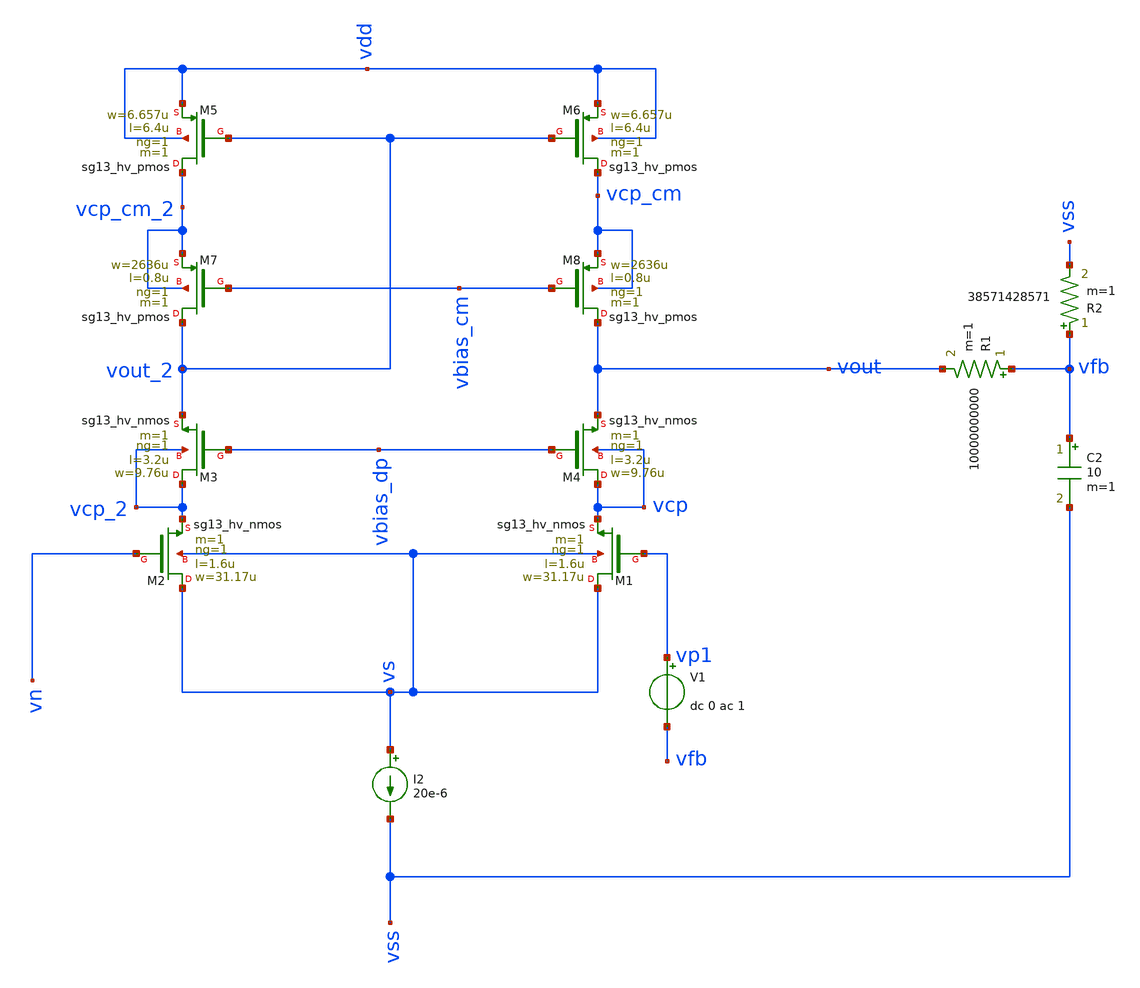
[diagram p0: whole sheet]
** sch_path: test/Tesis_notebooks/xschem/ota_tb_ihp_cc_full.sch
**.subckt ota_tb_ihp_cc_full
I2 vs vss 20e-6
XM1 vs vp1 vcp vs sg13_hv_nmos w=31.17u l=1.6u ng=1 m=1 mm_ok=1
XM2 vs vn vcp_2 vs sg13_hv_nmos w=31.17u l=1.6u ng=1 m=1 mm_ok=1
XM3 vcp_2 vbias_dp vout_2 vcp_2 sg13_hv_nmos w=9.76u l=3.2u ng=1 m=1 mm_ok=1
XM4 vcp vbias_dp vout vcp sg13_hv_nmos w=9.76u l=3.2u ng=1 m=1 mm_ok=1
XM5 vcp_cm_2 vout_2 vdd vdd sg13_hv_pmos w=6.657u l=6.4u ng=1 m=1 mm_ok=1
XM6 vcp_cm vout_2 vdd vdd sg13_hv_pmos w=6.657u l=6.4u ng=1 m=1 mm_ok=1
R1 vfb vout 10000000000 m=1
C2 vfb vss 10 m=1
R2 vfb vss 38571428571 m=1
V1 vp1 vfb dc 0 ac 1
XM7 vout_2 vbias_cm vcp_cm_2 vcp_cm_2 sg13_hv_pmos w=2636u l=0.8u ng=1 m=1 mm_ok=1
XM8 vout vbias_cm vcp_cm vcp_cm sg13_hv_pmos w=2636u l=0.8u ng=1 m=1 mm_ok=1
**** begin user architecture code



.lib /opt/pdks/ihp-sg13g2/libs.tech/ngspice/models/cornerMOShv.lib mos_tt

Vref vn 0 1.35
Vdd vdd 0 3.3
Vbias_dp vbias_dp 0 2.2
Vbias_cm vbias_cm vdd -0.88
Vss vss 0 0

.control
ac dec 10 1 1G



plot vdb(vout)
plot ph(vout)*180/PI
meas ac gain find vdb(vout) at=1
let low_gain = gain-3
meas ac fc WHEN vdb(vout)=low_gain

let phas = ph(vout)*180/PI

meas ac fu WHEN vdb(vout)=0
meas ac pmar find phas at=fu

op

let gm_m1 = @n.xm1.nsg13_hv_nmos[gm]
let gm_m2 = @n.xm2.nsg13_hv_nmos[gm]
let gm_m3 = @n.xm3.nsg13_hv_nmos[gm]
let gm_m4 = @n.xm4.nsg13_hv_nmos[gm]
let gm_m5 = @n.xm5.nsg13_hv_pmos[gm]
let gm_m6 = @n.xm6.nsg13_hv_pmos[gm]
let gm_m7 = @n.xm7.nsg13_hv_pmos[gm]
let gm_m8 = @n.xm8.nsg13_hv_pmos[gm]

let gds_m1 = @n.xm1.nsg13_hv_nmos[gds]
let gds_m2 = @n.xm2.nsg13_hv_nmos[gds]
let gds_m3 = @n.xm3.nsg13_hv_nmos[gds]
let gds_m4 = @n.xm4.nsg13_hv_nmos[gds]
let gds_m5 = @n.xm5.nsg13_hv_pmos[gds]
let gds_m6 = @n.xm6.nsg13_hv_pmos[gds]
let gds_m7 = @n.xm7.nsg13_hv_pmos[gds]
let gds_m8 = @n.xm8.nsg13_hv_pmos[gds]

let cds_m1 = abs(@n.xm1.nsg13_hv_nmos[cds])+abs(@n.xm1.nsg13_hv_nmos[cdb])
let cds_m4 = abs(@n.xm4.nsg13_hv_nmos[cds])+abs(@n.xm4.nsg13_hv_nmos[cdb])
let cds_m6 = abs(@n.xm6.nsg13_hv_pmos[cds])+abs(@n.xm6.nsg13_hv_pmos[cdb])
let cds_m8 = abs(@n.xm8.nsg13_hv_pmos[cds])+abs(@n.xm8.nsg13_hv_pmos[cdb])

let cgd_m1 = @n.xm1.nsg13_hv_nmos[cgd]
let cgd_m4 = @n.xm4.nsg13_hv_nmos[cgd]
let cgd_m6 = @n.xm6.nsg13_hv_pmos[cgd]
let cgd_m8 = @n.xm8.nsg13_hv_pmos[cgd]

let cgs_m1 = @n.xm1.nsg13_hv_nmos[cgg]
let cgs_m4 = @n.xm4.nsg13_hv_nmos[cgg]
let cgs_m6 = @n.xm6.nsg13_hv_pmos[cgg]
let cgs_m8 = @n.xm8.nsg13_hv_pmos[cgg]

let gain_cc1 = (gm_m3/gds_m3)
let gain_cc2 = (gm_m4/gds_m4)

let gain_cc3 = gm_m8/gds_m8
let gain_cc4 = gm_m7/gds_m7

let rout_diff1 = gain_cc1/gds_m1
let rout_diff2 = gain_cc2/gds_m2

let rout_cm1 = gain_cc3/gds_m6
let rout_cm2 = gain_cc4/gds_m5

print vout vs vcp vcp_2 vcp_cm vcp_cm_2 vout_2

print gm_m1
print gm_m2
print gm_m3
print gm_m4
print gm_m5
print gm_m6
print gm_m7
print gm_m8

print 1/gds_m1
print 1/gds_m2
print 1/gds_m3
print 1/gds_m4
print 1/gds_m5
print 1/gds_m6
print 1/gds_m7
print 1/gds_m8

print rout_diff1
print rout_diff2

print rout_cm1
print rout_cm2

print cds_m1
print cds_m4
print cds_m6
print cds_m8

print cgd_m1
print cgd_m4
print cgd_m6
print cgd_m8

print cgs_m1
print cgs_m4
print cgs_m6
print cgs_m8

.endc



**** end user architecture code
**.ends
.end
